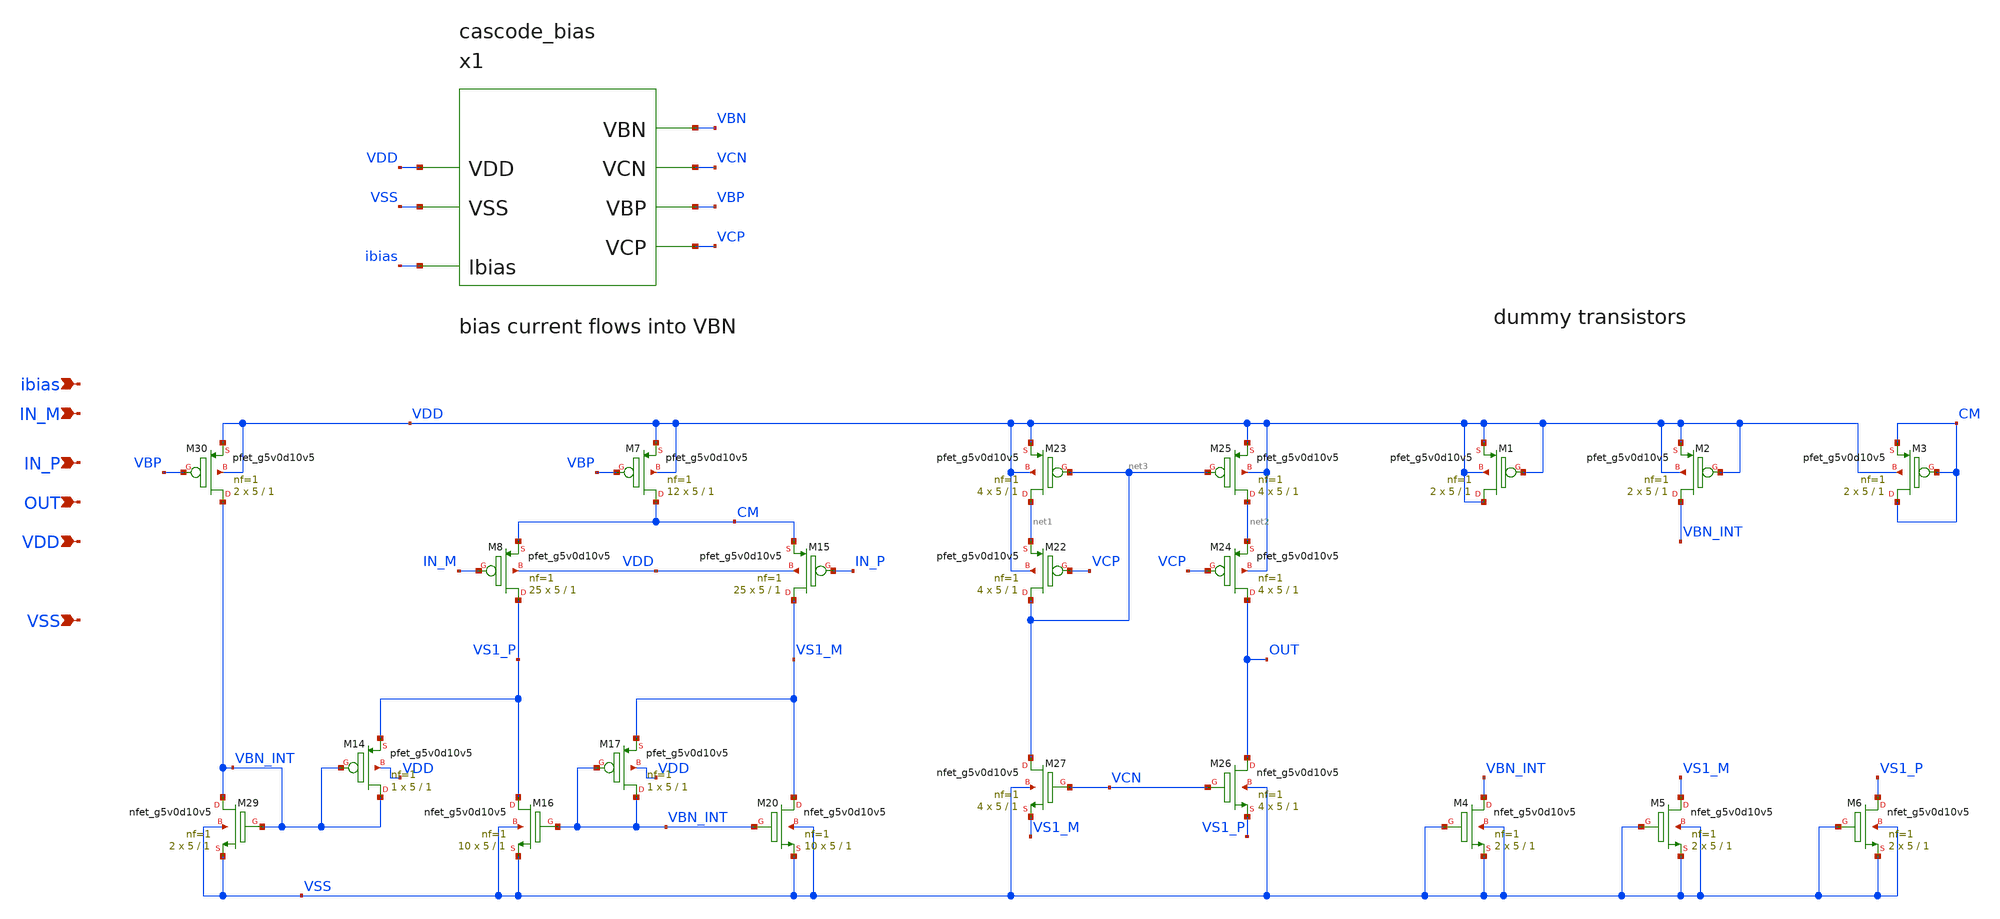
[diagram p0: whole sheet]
** sch_path: images/iic-osic-tools/addons/examples/open-pmic/design/folded-cascode-p-in/folded_cascode_p_in.sch
**.subckt folded_cascode_p_in ibias IN_M IN_P OUT VDD VSS
*.ipin ibias
*.ipin IN_M
*.ipin IN_P
*.ipin OUT
*.ipin VDD
*.ipin VSS
XM7 CM VBP VDD VDD sky130_fd_pr__pfet_g5v0d10v5 L=1 W=5 nf=1 ad='int((nf+1)/2) * W/nf * 0.29' as='int((nf+2)/2) * W/nf * 0.29'
+ pd='2*int((nf+1)/2) * (W/nf + 0.29)' ps='2*int((nf+2)/2) * (W/nf + 0.29)' nrd='0.29 / W' nrs='0.29 / W'
+ sa=0 sb=0 sd=0 mult=12 m=12
XM8 VS1_P IN_M CM VDD sky130_fd_pr__pfet_g5v0d10v5 L=1 W=5 nf=1 ad='int((nf+1)/2) * W/nf * 0.29' as='int((nf+2)/2) * W/nf * 0.29'
+ pd='2*int((nf+1)/2) * (W/nf + 0.29)' ps='2*int((nf+2)/2) * (W/nf + 0.29)' nrd='0.29 / W' nrs='0.29 / W'
+ sa=0 sb=0 sd=0 mult=25 m=25
XM15 VS1_M IN_P CM VDD sky130_fd_pr__pfet_g5v0d10v5 L=1 W=5 nf=1 ad='int((nf+1)/2) * W/nf * 0.29' as='int((nf+2)/2) * W/nf * 0.29'
+ pd='2*int((nf+1)/2) * (W/nf + 0.29)' ps='2*int((nf+2)/2) * (W/nf + 0.29)' nrd='0.29 / W' nrs='0.29 / W'
+ sa=0 sb=0 sd=0 mult=25 m=25
XM16 VS1_P VBN_INT VSS VSS sky130_fd_pr__nfet_g5v0d10v5 L=1 W=5 nf=1 ad='int((nf+1)/2) * W/nf * 0.29'
+ as='int((nf+2)/2) * W/nf * 0.29' pd='2*int((nf+1)/2) * (W/nf + 0.29)' ps='2*int((nf+2)/2) * (W/nf + 0.29)'
+ nrd='0.29 / W' nrs='0.29 / W' sa=0 sb=0 sd=0 mult=10 m=10
XM20 VS1_M VBN_INT VSS VSS sky130_fd_pr__nfet_g5v0d10v5 L=1 W=5 nf=1 ad='int((nf+1)/2) * W/nf * 0.29'
+ as='int((nf+2)/2) * W/nf * 0.29' pd='2*int((nf+1)/2) * (W/nf + 0.29)' ps='2*int((nf+2)/2) * (W/nf + 0.29)'
+ nrd='0.29 / W' nrs='0.29 / W' sa=0 sb=0 sd=0 mult=10 m=10
XM22 net3 VCP net1 VDD sky130_fd_pr__pfet_g5v0d10v5 L=1 W=5 nf=1 ad='int((nf+1)/2) * W/nf * 0.29' as='int((nf+2)/2) * W/nf * 0.29'
+ pd='2*int((nf+1)/2) * (W/nf + 0.29)' ps='2*int((nf+2)/2) * (W/nf + 0.29)' nrd='0.29 / W' nrs='0.29 / W'
+ sa=0 sb=0 sd=0 mult=4 m=4
XM23 net1 net3 VDD VDD sky130_fd_pr__pfet_g5v0d10v5 L=1 W=5 nf=1 ad='int((nf+1)/2) * W/nf * 0.29' as='int((nf+2)/2) * W/nf * 0.29'
+ pd='2*int((nf+1)/2) * (W/nf + 0.29)' ps='2*int((nf+2)/2) * (W/nf + 0.29)' nrd='0.29 / W' nrs='0.29 / W'
+ sa=0 sb=0 sd=0 mult=4 m=4
XM24 OUT VCP net2 VDD sky130_fd_pr__pfet_g5v0d10v5 L=1 W=5 nf=1 ad='int((nf+1)/2) * W/nf * 0.29' as='int((nf+2)/2) * W/nf * 0.29'
+ pd='2*int((nf+1)/2) * (W/nf + 0.29)' ps='2*int((nf+2)/2) * (W/nf + 0.29)' nrd='0.29 / W' nrs='0.29 / W'
+ sa=0 sb=0 sd=0 mult=4 m=4
XM25 net2 net3 VDD VDD sky130_fd_pr__pfet_g5v0d10v5 L=1 W=5 nf=1 ad='int((nf+1)/2) * W/nf * 0.29' as='int((nf+2)/2) * W/nf * 0.29'
+ pd='2*int((nf+1)/2) * (W/nf + 0.29)' ps='2*int((nf+2)/2) * (W/nf + 0.29)' nrd='0.29 / W' nrs='0.29 / W'
+ sa=0 sb=0 sd=0 mult=4 m=4
XM26 OUT VCN VS1_P VSS sky130_fd_pr__nfet_g5v0d10v5 L=1 W=5 nf=1 ad='int((nf+1)/2) * W/nf * 0.29' as='int((nf+2)/2) * W/nf * 0.29'
+ pd='2*int((nf+1)/2) * (W/nf + 0.29)' ps='2*int((nf+2)/2) * (W/nf + 0.29)' nrd='0.29 / W' nrs='0.29 / W'
+ sa=0 sb=0 sd=0 mult=4 m=4
XM27 net3 VCN VS1_M VSS sky130_fd_pr__nfet_g5v0d10v5 L=1 W=5 nf=1 ad='int((nf+1)/2) * W/nf * 0.29' as='int((nf+2)/2) * W/nf * 0.29'
+ pd='2*int((nf+1)/2) * (W/nf + 0.29)' ps='2*int((nf+2)/2) * (W/nf + 0.29)' nrd='0.29 / W' nrs='0.29 / W'
+ sa=0 sb=0 sd=0 mult=4 m=4
XM29 VBN_INT VBN_INT VSS VSS sky130_fd_pr__nfet_g5v0d10v5 L=1 W=5 nf=1 ad='int((nf+1)/2) * W/nf * 0.29'
+ as='int((nf+2)/2) * W/nf * 0.29' pd='2*int((nf+1)/2) * (W/nf + 0.29)' ps='2*int((nf+2)/2) * (W/nf + 0.29)'
+ nrd='0.29 / W' nrs='0.29 / W' sa=0 sb=0 sd=0 mult=2 m=2
XM30 VBN_INT VBP VDD VDD sky130_fd_pr__pfet_g5v0d10v5 L=1 W=5 nf=1 ad='int((nf+1)/2) * W/nf * 0.29' as='int((nf+2)/2) * W/nf * 0.29'
+ pd='2*int((nf+1)/2) * (W/nf + 0.29)' ps='2*int((nf+2)/2) * (W/nf + 0.29)' nrd='0.29 / W' nrs='0.29 / W'
+ sa=0 sb=0 sd=0 mult=2 m=2
XM14 VBN_INT VBN_INT VS1_P VDD sky130_fd_pr__pfet_g5v0d10v5 L=1 W=5 nf=1 ad='int((nf+1)/2) * W/nf * 0.29'
+ as='int((nf+2)/2) * W/nf * 0.29' pd='2*int((nf+1)/2) * (W/nf + 0.29)' ps='2*int((nf+2)/2) * (W/nf + 0.29)'
+ nrd='0.29 / W' nrs='0.29 / W' sa=0 sb=0 sd=0 mult=1 m=1
XM17 VBN_INT VBN_INT VS1_M VDD sky130_fd_pr__pfet_g5v0d10v5 L=1 W=5 nf=1 ad='int((nf+1)/2) * W/nf * 0.29'
+ as='int((nf+2)/2) * W/nf * 0.29' pd='2*int((nf+1)/2) * (W/nf + 0.29)' ps='2*int((nf+2)/2) * (W/nf + 0.29)'
+ nrd='0.29 / W' nrs='0.29 / W' sa=0 sb=0 sd=0 mult=1 m=1
x1 VBN VCN VBP VCP VDD VSS ibias cascode_bias
XM1 VDD VDD VDD VDD sky130_fd_pr__pfet_g5v0d10v5 L=1 W=5 nf=1 ad='int((nf+1)/2) * W/nf * 0.29' as='int((nf+2)/2) * W/nf * 0.29'
+ pd='2*int((nf+1)/2) * (W/nf + 0.29)' ps='2*int((nf+2)/2) * (W/nf + 0.29)' nrd='0.29 / W' nrs='0.29 / W'
+ sa=0 sb=0 sd=0 mult=2 m=2
XM2 VBN_INT VDD VDD VDD sky130_fd_pr__pfet_g5v0d10v5 L=1 W=5 nf=1 ad='int((nf+1)/2) * W/nf * 0.29' as='int((nf+2)/2) * W/nf * 0.29'
+ pd='2*int((nf+1)/2) * (W/nf + 0.29)' ps='2*int((nf+2)/2) * (W/nf + 0.29)' nrd='0.29 / W' nrs='0.29 / W'
+ sa=0 sb=0 sd=0 mult=2 m=2
XM3 CM CM CM VDD sky130_fd_pr__pfet_g5v0d10v5 L=1 W=5 nf=1 ad='int((nf+1)/2) * W/nf * 0.29' as='int((nf+2)/2) * W/nf * 0.29'
+ pd='2*int((nf+1)/2) * (W/nf + 0.29)' ps='2*int((nf+2)/2) * (W/nf + 0.29)' nrd='0.29 / W' nrs='0.29 / W'
+ sa=0 sb=0 sd=0 mult=2 m=2
XM4 VBN_INT VSS VSS VSS sky130_fd_pr__nfet_g5v0d10v5 L=1 W=5 nf=1 ad='int((nf+1)/2) * W/nf * 0.29' as='int((nf+2)/2) * W/nf * 0.29'
+ pd='2*int((nf+1)/2) * (W/nf + 0.29)' ps='2*int((nf+2)/2) * (W/nf + 0.29)' nrd='0.29 / W' nrs='0.29 / W'
+ sa=0 sb=0 sd=0 mult=2 m=2
XM5 VS1_M VSS VSS VSS sky130_fd_pr__nfet_g5v0d10v5 L=1 W=5 nf=1 ad='int((nf+1)/2) * W/nf * 0.29' as='int((nf+2)/2) * W/nf * 0.29'
+ pd='2*int((nf+1)/2) * (W/nf + 0.29)' ps='2*int((nf+2)/2) * (W/nf + 0.29)' nrd='0.29 / W' nrs='0.29 / W'
+ sa=0 sb=0 sd=0 mult=2 m=2
XM6 VS1_P VSS VSS VSS sky130_fd_pr__nfet_g5v0d10v5 L=1 W=5 nf=1 ad='int((nf+1)/2) * W/nf * 0.29' as='int((nf+2)/2) * W/nf * 0.29'
+ pd='2*int((nf+1)/2) * (W/nf + 0.29)' ps='2*int((nf+2)/2) * (W/nf + 0.29)' nrd='0.29 / W' nrs='0.29 / W'
+ sa=0 sb=0 sd=0 mult=2 m=2
**.ends
.end
